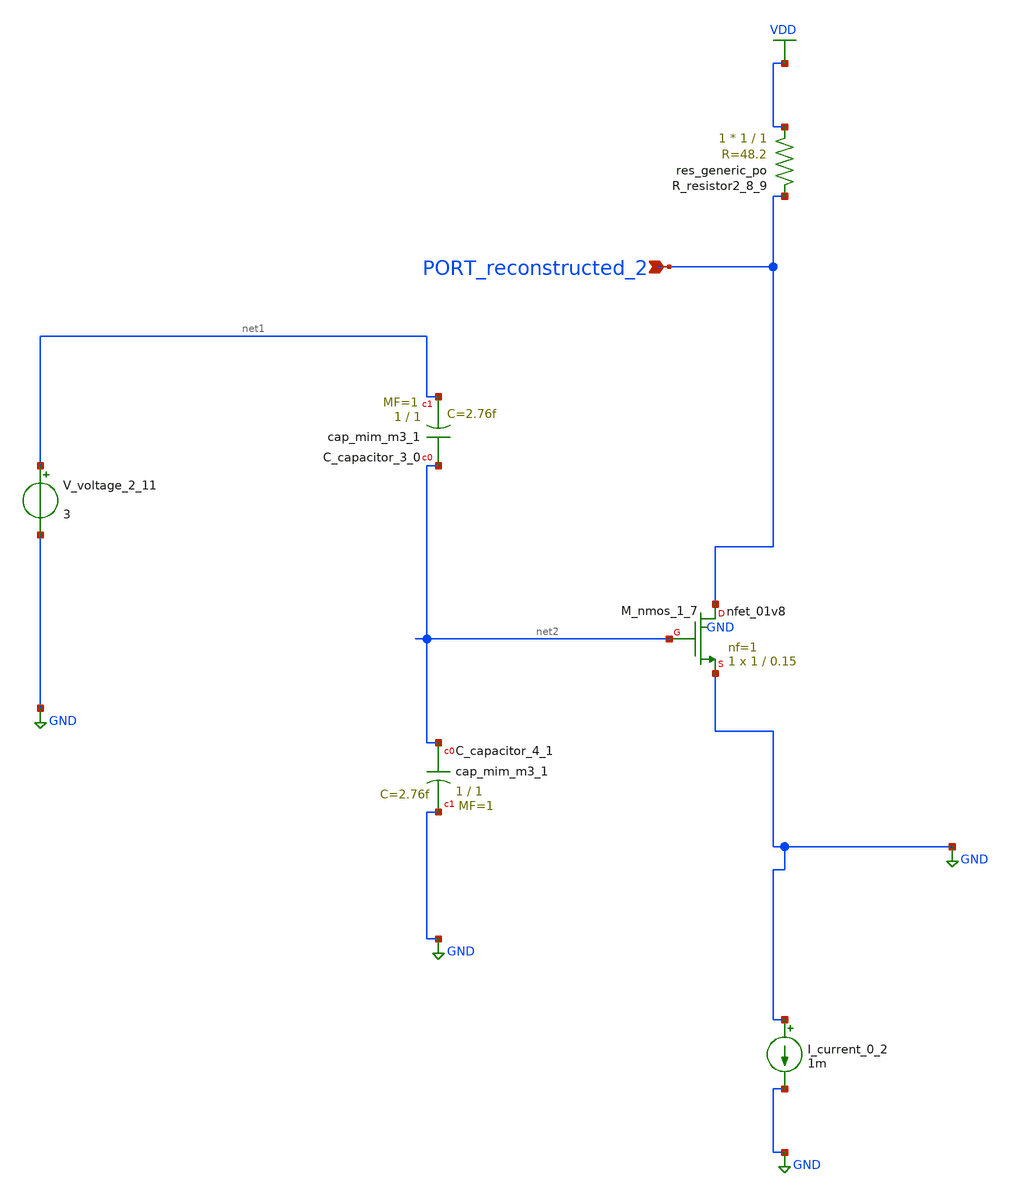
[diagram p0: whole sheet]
** sch_path: schematics/AMSNet/557.sch
**.subckt 557 PORT_reconstructed_2
*.ipin PORT_reconstructed_2
XC_capacitor_3_0 net2 net1 sky130_fd_pr__cap_mim_m3_1 W=1 L=1 MF=1 m=1
XC_capacitor_4_1 net2 GND sky130_fd_pr__cap_mim_m3_1 W=1 L=1 MF=1 m=1
I_current_0_2 GND GND 1m
XM_nmos_1_7 PORT_reconstructed_2 net2 GND GND sky130_fd_pr__nfet_01v8 L=0.15 W=1 nf=1 ad='int((1 + 1)/2) * 1 / 1 * 0.29'
+ as='int((1 + 2)/2) * 1 / 1 * 0.29' pd='2*int((1 + 1)/2) * (1 / 1 + 0.29)' ps='2*int((1 + 2)/2) * (1 / 1 + 0.29)'
+ nrd='0.29 / 1 ' nrs='0.29 / 1 ' sa=0 sb=0 sd=0 mult=1 m=1
XR_resistor2_8_9 VDD PORT_reconstructed_2 sky130_fd_pr__res_generic_po W=1 L=1 m=1
V_voltage_2_11 net1 GND 3
**.ends
.GLOBAL GND
.GLOBAL VDD
.end
